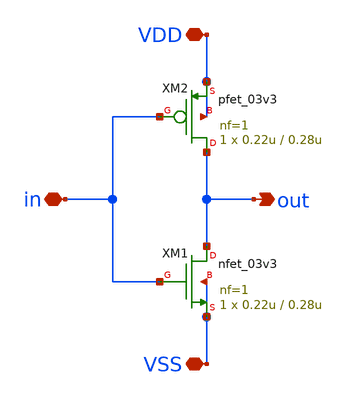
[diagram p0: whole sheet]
** sch_path: designs/sar_adc/digital/inverter/xschem/inverter.sch
**.subckt inverter out in VDD VSS
*.opin out
*.iopin in
*.iopin VDD
*.iopin VSS
XM1 out in VSS VSS nfet_03v3 L=0.28u W=0.22u nf=1 ad='int((nf+1)/2) * W/nf * 0.18u' as='int((nf+2)/2) * W/nf * 0.18u'
+ pd='2*int((nf+1)/2) * (W/nf + 0.18u)' ps='2*int((nf+2)/2) * (W/nf + 0.18u)' nrd='0.18u / W' nrs='0.18u / W'
+ sa=0 sb=0 sd=0 m=1
XM2 out in VDD VDD pfet_03v3 L=0.28u W=0.22u nf=1 ad='int((nf+1)/2) * W/nf * 0.18u' as='int((nf+2)/2) * W/nf * 0.18u'
+ pd='2*int((nf+1)/2) * (W/nf + 0.18u)' ps='2*int((nf+2)/2) * (W/nf + 0.18u)' nrd='0.18u / W' nrs='0.18u / W'
+ sa=0 sb=0 sd=0 m=1
**.ends
.end
